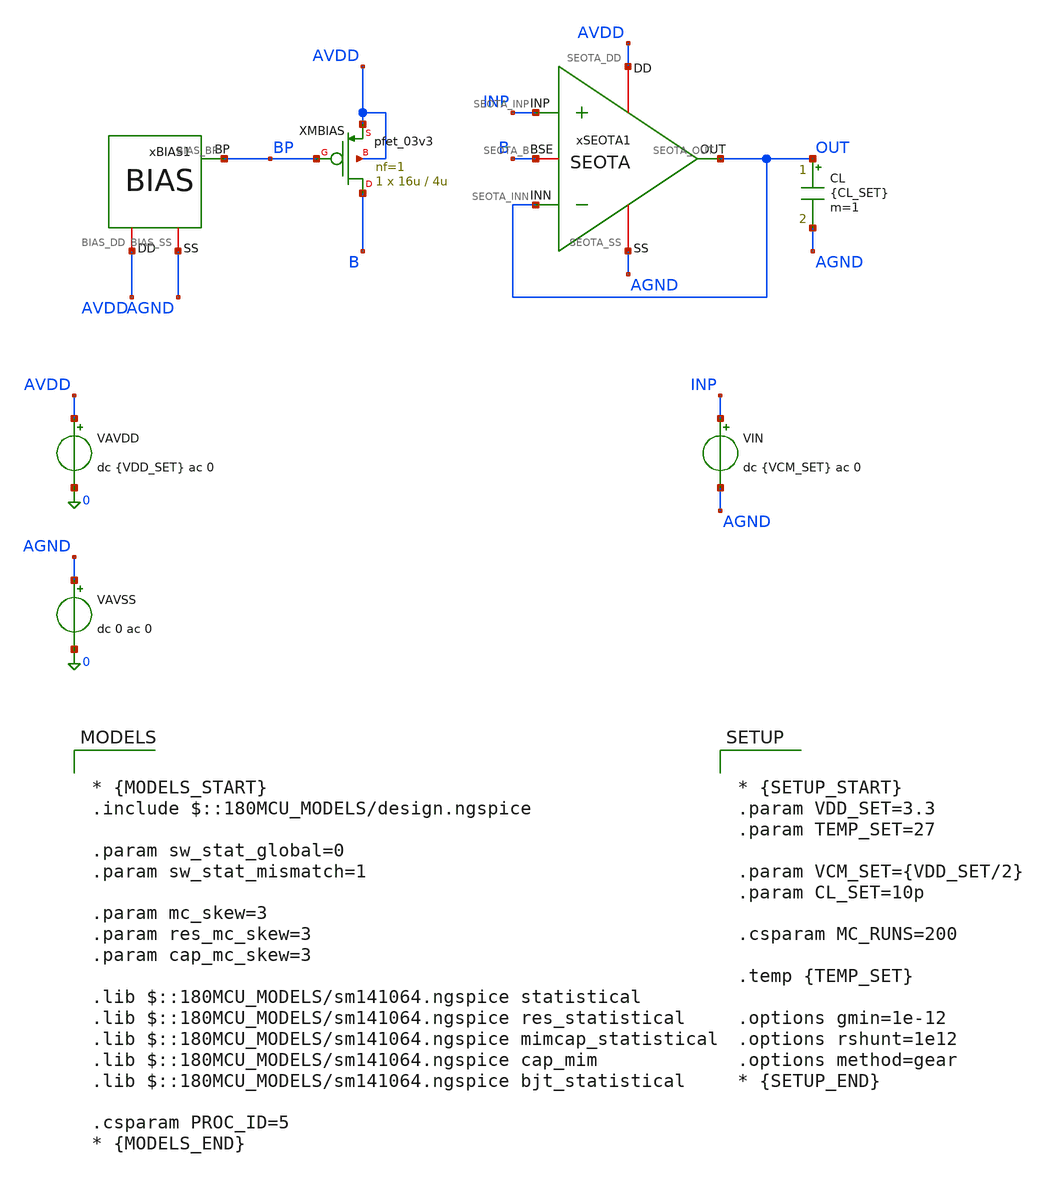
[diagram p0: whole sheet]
** sch_path: Design_Files/IC Design/Testbench/ANALOG_BLOCKS/SEOTA/Close_Loop/SEOTA_TB_CL_MC.sch
**.subckt SEOTA_TB_CL_MC
CL OUT AGND {CL_SET} m=1
xSEOTA1 AVDD AGND INP OUT OUT B SEOTA
VAVDD AVDD 0 dc {VDD_SET} ac 0
.save i(vavdd)
VIN INP AGND dc {VCM_SET} ac 0
VAVSS AGND 0 dc 0 ac 0
xBIAS1 AVDD AGND BP BIAS
XMBIAS B BP AVDD AVDD pfet_03v3 L=4u W=16u nf=1 ad='int((nf+1)/2) * W/nf * 0.18u' as='int((nf+2)/2) * W/nf * 0.18u'
+ pd='2*int((nf+1)/2) * (W/nf + 0.18u)' ps='2*int((nf+2)/2) * (W/nf + 0.18u)' nrd='0.18u / W' nrs='0.18u / W'
+ sa=0 sb=0 sd=0 m=1
**** begin user architecture code

* {MODELS_START}
.include $::180MCU_MODELS/design.ngspice

.param sw_stat_global=0
.param sw_stat_mismatch=1

.param mc_skew=3
.param res_mc_skew=3
.param cap_mc_skew=3

.lib $::180MCU_MODELS/sm141064.ngspice statistical
.lib $::180MCU_MODELS/sm141064.ngspice res_statistical
.lib $::180MCU_MODELS/sm141064.ngspice mimcap_statistical
.lib $::180MCU_MODELS/sm141064.ngspice cap_mim
.lib $::180MCU_MODELS/sm141064.ngspice bjt_statistical

.csparam PROC_ID=5
* {MODELS_END}



* {SETUP_START}
.param VDD_SET=3.3
.param TEMP_SET=27

.param VCM_SET={VDD_SET/2}
.param CL_SET=10p

.csparam MC_RUNS=200

.temp {TEMP_SET}

.options gmin=1e-12
.options rshunt=1e12
.options method=gear
* {SETUP_END}




* {MEAS_START}

.control

destroy all

set noaskquit
set wr_singlescale
unset wr_vecnames

option klu
option numdgt=15
option method=gear
option maxord=2
option plotwinsize=0


let mode_index=0
dowhile mode_index < 3
if mode_index = 0
set proc=MM
alterparam sw_stat_global=0
alterparam sw_stat_mismatch=1
end
if mode_index = 1
set proc=GL
alterparam sw_stat_global=1
alterparam sw_stat_mismatch=0
end
if mode_index = 2
set proc=FULL
alterparam sw_stat_global=1
alterparam sw_stat_mismatch=1
end
reset

shell mkdir -p /foss/designs/ECG_Acquisition_IC/Measurement_Results/IC_Simulation/ANALOG_BLOCKS/SEOTA/{$proc}.Result_txt

shell rm -f /foss/designs/ECG_Acquisition_IC/Measurement_Results/IC_Simulation/ANALOG_BLOCKS/SEOTA/{$proc}.Result_txt/{$proc}.cl_mc_summary.txt
shell rm -f /foss/designs/ECG_Acquisition_IC/Measurement_Results/IC_Simulation/ANALOG_BLOCKS/SEOTA/{$proc}.Result_txt/{$proc}.cl_mc_debug_op.txt


echo run vos_V vout_V out_error_V cl_gain_10 b_V ibias_A idd_A power_W > /foss/designs/ECG_Acquisition_IC/Measurement_Results/IC_Simulation/ANALOG_BLOCKS/SEOTA/{$proc}.Result_txt/{$proc}.cl_mc_summary.txt

echo run vin_V vout_V vos_V net1_V net2_V net3_V net4_V b_V ibias_A idd_A power_W > /foss/designs/ECG_Acquisition_IC/Measurement_Results/IC_Simulation/ANALOG_BLOCKS/SEOTA/{$proc}.Result_txt/{$proc}.cl_mc_debug_op.txt


let run=1
let mc_runs=$&MC_RUNS


dowhile run <= mc_runs


set runnum=$&run

setseed $runnum
mc_source

option klu
option numdgt=15
option method=gear
option maxord=2
option plotwinsize=0

save all
save @m.xmbias.m0[id]


* OP

op

let vin_op=v(INP)-v(AGND)
let vout_op=v(OUT)-v(AGND)

let vos=vin_op-vout_op
let out_error=vout_op-vin_op

let b_op=v(B)-v(AGND)

let net1_op=v(xseota1.net1)-v(AGND)
let net2_op=v(xseota1.net2)-v(AGND)
let net3_op=v(xseota1.net3)-v(AGND)
let net4_op=v(xseota1.net4)-v(AGND)

let ibias=abs(@m.xmbias.m0[id])
let idd_total=abs(vavdd#branch)
let power_total=(v(AVDD)-v(AGND))*idd_total


set vin_val=$&vin_op
set vout_val=$&vout_op

set vos_val=$&vos
set out_error_val=$&out_error

set b_val=$&b_op

set net1_val=$&net1_op
set net2_val=$&net2_op
set net3_val=$&net3_op
set net4_val=$&net4_op

set ibias_val=$&ibias
set idd_val=$&idd_total
set power_val=$&power_total


echo $runnum $vin_val $vout_val $vos_val $net1_val $net2_val $net3_val $net4_val $b_val $ibias_val $idd_val
+ $power_val >> /foss/designs/ECG_Acquisition_IC/Measurement_Results/IC_Simulation/ANALOG_BLOCKS/SEOTA/{$proc}.Result_txt/{$proc}.cl_mc_debug_op.txt


destroy all


* CLOSED-LOOP AC

alter @VIN[ACMAG]=1
alter @VIN[ACPHASE]=0

ac dec 100 0.1 10Meg

let vin_ac=v(INP)-v(AGND)
let vout_ac=v(OUT)-v(AGND)

let cl_tf=vout_ac/vin_ac
let cl_gain=mag(cl_tf)

meas ac cl_gain_10 find cl_gain at=10

set cl_gain_val=$&cl_gain_10


* SUMMARY

echo $runnum $vos_val $vout_val $out_error_val $cl_gain_val $b_val $ibias_val $idd_val $power_val >>
+ /foss/designs/ECG_Acquisition_IC/Measurement_Results/IC_Simulation/ANALOG_BLOCKS/SEOTA/{$proc}.Result_txt/{$proc}.cl_mc_summary.txt


destroy all

let run=run+1


end


let mode_index=mode_index+1
end

quit

.endc
* {MEAS_END}


**** end user architecture code
**.ends
.end
